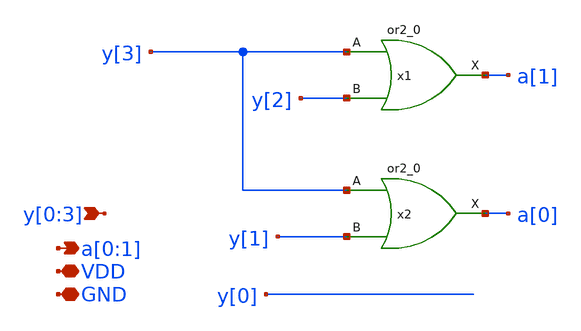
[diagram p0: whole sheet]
** sch_path: design/xschem/encoder_4_to_2.sch
**.subckt encoder_4_to_2 a[0],a[1] y[0],y[1],y[2],y[3] VDD GND
*.opin a[0],a[1]
*.ipin y[0],y[1],y[2],y[3]
*.iopin VDD
*.iopin GND
x1 y[3] y[2] GND GND VDD VDD a[1] sky130_fd_sc_hd__or2_0
x2 y[3] y[1] GND GND VDD VDD a[0] sky130_fd_sc_hd__or2_0
**.ends
.end
